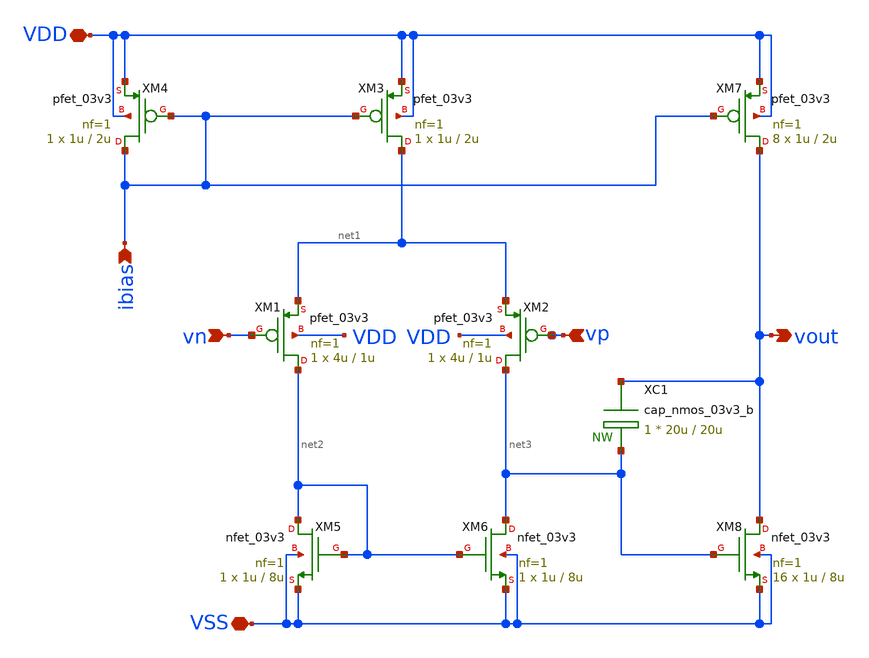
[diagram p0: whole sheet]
** sch_path: designs/libs/core_analog/opamp_two_stage/opamp_two_stage.sch
**.subckt opamp_two_stage vn vp vout ibias VDD VSS
*.ipin vn
*.ipin vp
*.opin vout
*.ipin ibias
*.iopin VDD
*.iopin VSS
XM1 net2 vn net1 VDD pfet_03v3 L=1u W=4u nf=1 ad='int((nf+1)/2) * W/nf * 0.18u' as='int((nf+2)/2) * W/nf * 0.18u'
+ pd='2*int((nf+1)/2) * (W/nf + 0.18u)' ps='2*int((nf+2)/2) * (W/nf + 0.18u)' nrd='0.18u / W' nrs='0.18u / W'
+ sa=0 sb=0 sd=0 m=1
XM2 net3 vp net1 VDD pfet_03v3 L=1u W=4u nf=1 ad='int((nf+1)/2) * W/nf * 0.18u' as='int((nf+2)/2) * W/nf * 0.18u'
+ pd='2*int((nf+1)/2) * (W/nf + 0.18u)' ps='2*int((nf+2)/2) * (W/nf + 0.18u)' nrd='0.18u / W' nrs='0.18u / W'
+ sa=0 sb=0 sd=0 m=1
XM3 net1 ibias VDD VDD pfet_03v3 L=2u W=1u nf=1 ad='int((nf+1)/2) * W/nf * 0.18u' as='int((nf+2)/2) * W/nf * 0.18u'
+ pd='2*int((nf+1)/2) * (W/nf + 0.18u)' ps='2*int((nf+2)/2) * (W/nf + 0.18u)' nrd='0.18u / W' nrs='0.18u / W'
+ sa=0 sb=0 sd=0 m=1
XM4 ibias ibias VDD VDD pfet_03v3 L=2u W=1u nf=1 ad='int((nf+1)/2) * W/nf * 0.18u' as='int((nf+2)/2) * W/nf * 0.18u'
+ pd='2*int((nf+1)/2) * (W/nf + 0.18u)' ps='2*int((nf+2)/2) * (W/nf + 0.18u)' nrd='0.18u / W' nrs='0.18u / W'
+ sa=0 sb=0 sd=0 m=1
XM5 net2 net2 VSS VSS nfet_03v3 L=8u W=1u nf=1 ad='int((nf+1)/2) * W/nf * 0.18u' as='int((nf+2)/2) * W/nf * 0.18u'
+ pd='2*int((nf+1)/2) * (W/nf + 0.18u)' ps='2*int((nf+2)/2) * (W/nf + 0.18u)' nrd='0.18u / W' nrs='0.18u / W'
+ sa=0 sb=0 sd=0 m=1
XM6 net3 net2 VSS VSS nfet_03v3 L=8u W=1u nf=1 ad='int((nf+1)/2) * W/nf * 0.18u' as='int((nf+2)/2) * W/nf * 0.18u'
+ pd='2*int((nf+1)/2) * (W/nf + 0.18u)' ps='2*int((nf+2)/2) * (W/nf + 0.18u)' nrd='0.18u / W' nrs='0.18u / W'
+ sa=0 sb=0 sd=0 m=1
XM7 vout ibias VDD VDD pfet_03v3 L=2u W=1u nf=1 ad='int((nf+1)/2) * W/nf * 0.18u' as='int((nf+2)/2) * W/nf * 0.18u'
+ pd='2*int((nf+1)/2) * (W/nf + 0.18u)' ps='2*int((nf+2)/2) * (W/nf + 0.18u)' nrd='0.18u / W' nrs='0.18u / W'
+ sa=0 sb=0 sd=0 m=8
XM8 vout net3 VSS VSS nfet_03v3 L=8u W=1u nf=1 ad='int((nf+1)/2) * W/nf * 0.18u' as='int((nf+2)/2) * W/nf * 0.18u'
+ pd='2*int((nf+1)/2) * (W/nf + 0.18u)' ps='2*int((nf+2)/2) * (W/nf + 0.18u)' nrd='0.18u / W' nrs='0.18u / W'
+ sa=0 sb=0 sd=0 m=16
XC1 vout net3 cap_nmos_03v3_b c_width=20u c_length=20u m=1
**.ends
.end
